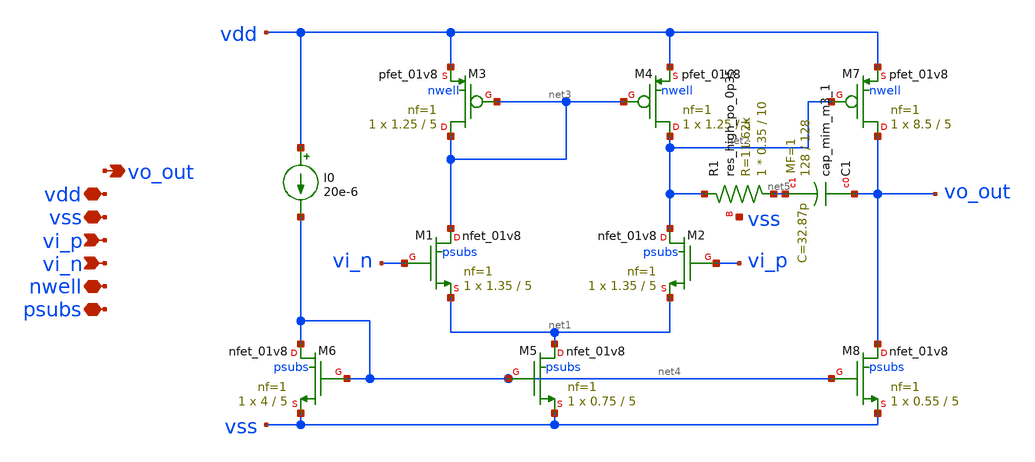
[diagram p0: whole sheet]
** sch_path: xschem/op.sch
**.subckt op vss vdd vo_out vi_p vi_n psubs nwell
*.iopin vss
*.iopin vdd
*.opin vo_out
*.ipin vi_p
*.ipin vi_n
*.iopin psubs
*.iopin nwell
XM1 net3 vi_n net1 psubs sky130_fd_pr__nfet_01v8 L=5 W=1.35 nf=1 ad='int((nf+1)/2) * W/nf * 0.29' as='int((nf+2)/2) * W/nf * 0.29'
+ pd='2*int((nf+1)/2) * (W/nf + 0.29)' ps='2*int((nf+2)/2) * (W/nf + 0.29)' nrd='0.29 / W' nrs='0.29 / W'
+ sa=0 sb=0 sd=0 mult=1 m=1
XM3 net3 net3 vdd nwell sky130_fd_pr__pfet_01v8 L=5 W=1.25 nf=1 ad='int((1 + 1)/2) * 1.25 / 1 * 0.29'
+ as='int((1 + 2)/2) * 1.25 / 1 * 0.29' pd='2*int((1 + 1)/2) * (1.25 / 1 + 0.29)' ps='2*int((1 + 2)/2) * (1.25 / 1 + 0.29)'
+ nrd='0.29 / 1.25 ' nrs='0.29 / 1.25 ' sa=0 sb=0 sd=0 mult=1 m=1
XM6 net4 net4 vss psubs sky130_fd_pr__nfet_01v8 L=5 W=4 nf=1 ad='int((1 + 1)/2) * 4 / 1 * 0.29' as='int((1 + 2)/2) * 4 / 1 * 0.29'
+ pd='2*int((1 + 1)/2) * (4 / 1 + 0.29)' ps='2*int((1 + 2)/2) * (4 / 1 + 0.29)' nrd='0.29 / 4 ' nrs='0.29 / 4 '
+ sa=0 sb=0 sd=0 mult=1 m=1
I0 vdd net4 20e-6
XM5 net1 net4 vss psubs sky130_fd_pr__nfet_01v8 L=5 W=0.75 nf=1 ad='int((1 + 1)/2) * 0.75 / 1 * 0.29'
+ as='int((1 + 2)/2) * 0.75 / 1 * 0.29' pd='2*int((1 + 1)/2) * (0.75 / 1 + 0.29)' ps='2*int((1 + 2)/2) * (0.75 / 1 + 0.29)'
+ nrd='0.29 / 0.75 ' nrs='0.29 / 0.75 ' sa=0 sb=0 sd=0 mult=1 m=1
XM7 vo_out net2 vdd nwell sky130_fd_pr__pfet_01v8 L=5 W=8.5 nf=1 ad='int((1 + 1)/2) * 8.5 / 1 * 0.29'
+ as='int((1 + 2)/2) * 8.5 / 1 * 0.29' pd='2*int((1 + 1)/2) * (8.5 / 1 + 0.29)' ps='2*int((1 + 2)/2) * (8.5 / 1 + 0.29)'
+ nrd='0.29 / 8.5 ' nrs='0.29 / 8.5 ' sa=0 sb=0 sd=0 mult=1 m=1
XM8 vo_out net4 vss psubs sky130_fd_pr__nfet_01v8 L=5 W=0.55 nf=1 ad='int((1 + 1)/2) * 0.55 / 1 * 0.29'
+ as='int((1 + 2)/2) * 0.55 / 1 * 0.29' pd='2*int((1 + 1)/2) * (0.55 / 1 + 0.29)' ps='2*int((1 + 2)/2) * (0.55 / 1 + 0.29)'
+ nrd='0.29 / 0.55 ' nrs='0.29 / 0.55 ' sa=0 sb=0 sd=0 mult=1 m=1
XM2 net2 vi_p net1 psubs sky130_fd_pr__nfet_01v8 L=5 W=1.35 nf=1 ad='int((nf+1)/2) * W/nf * 0.29' as='int((nf+2)/2) * W/nf * 0.29'
+ pd='2*int((nf+1)/2) * (W/nf + 0.29)' ps='2*int((nf+2)/2) * (W/nf + 0.29)' nrd='0.29 / W' nrs='0.29 / W'
+ sa=0 sb=0 sd=0 mult=1 m=1
XM4 net2 net3 vdd nwell sky130_fd_pr__pfet_01v8 L=5 W=1.25 nf=1 ad='int((1 + 1)/2) * 1.25 / 1 * 0.29'
+ as='int((1 + 2)/2) * 1.25 / 1 * 0.29' pd='2*int((1 + 1)/2) * (1.25 / 1 + 0.29)' ps='2*int((1 + 2)/2) * (1.25 / 1 + 0.29)'
+ nrd='0.29 / 1.25 ' nrs='0.29 / 1.25 ' sa=0 sb=0 sd=0 mult=1 m=1
XR1 net5 net2 vss sky130_fd_pr__res_high_po_0p35 L=10 mult=1 m=1
XC1 vo_out net5 sky130_fd_pr__cap_mim_m3_1 W=128 L=128 MF=1 m=1
**** begin user architecture code


.include ./sizing_opamp.spice


**** end user architecture code
**.ends
.end
